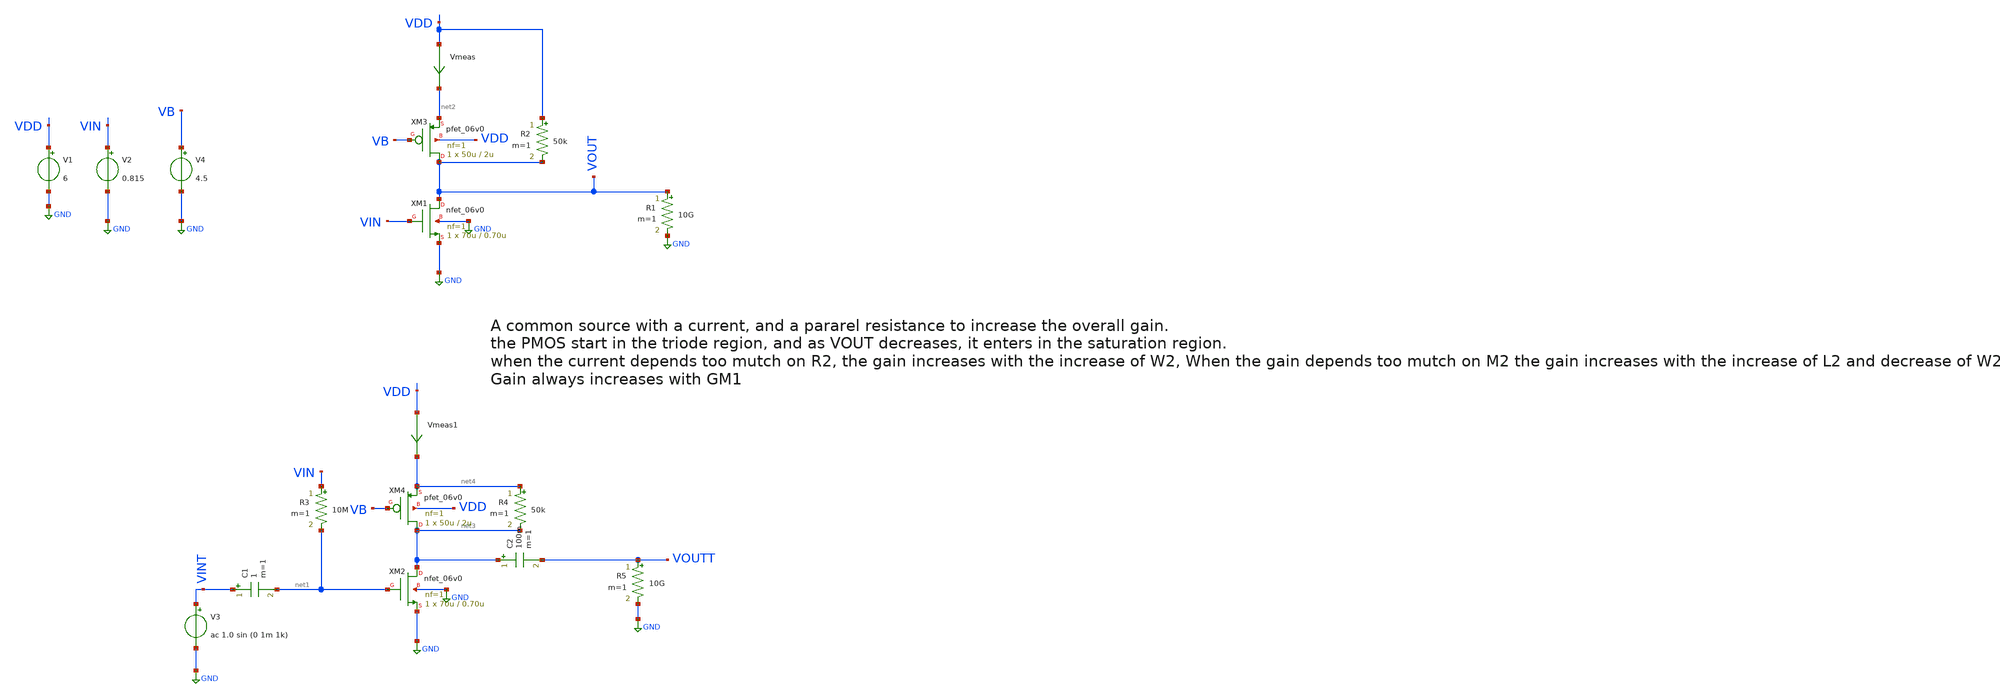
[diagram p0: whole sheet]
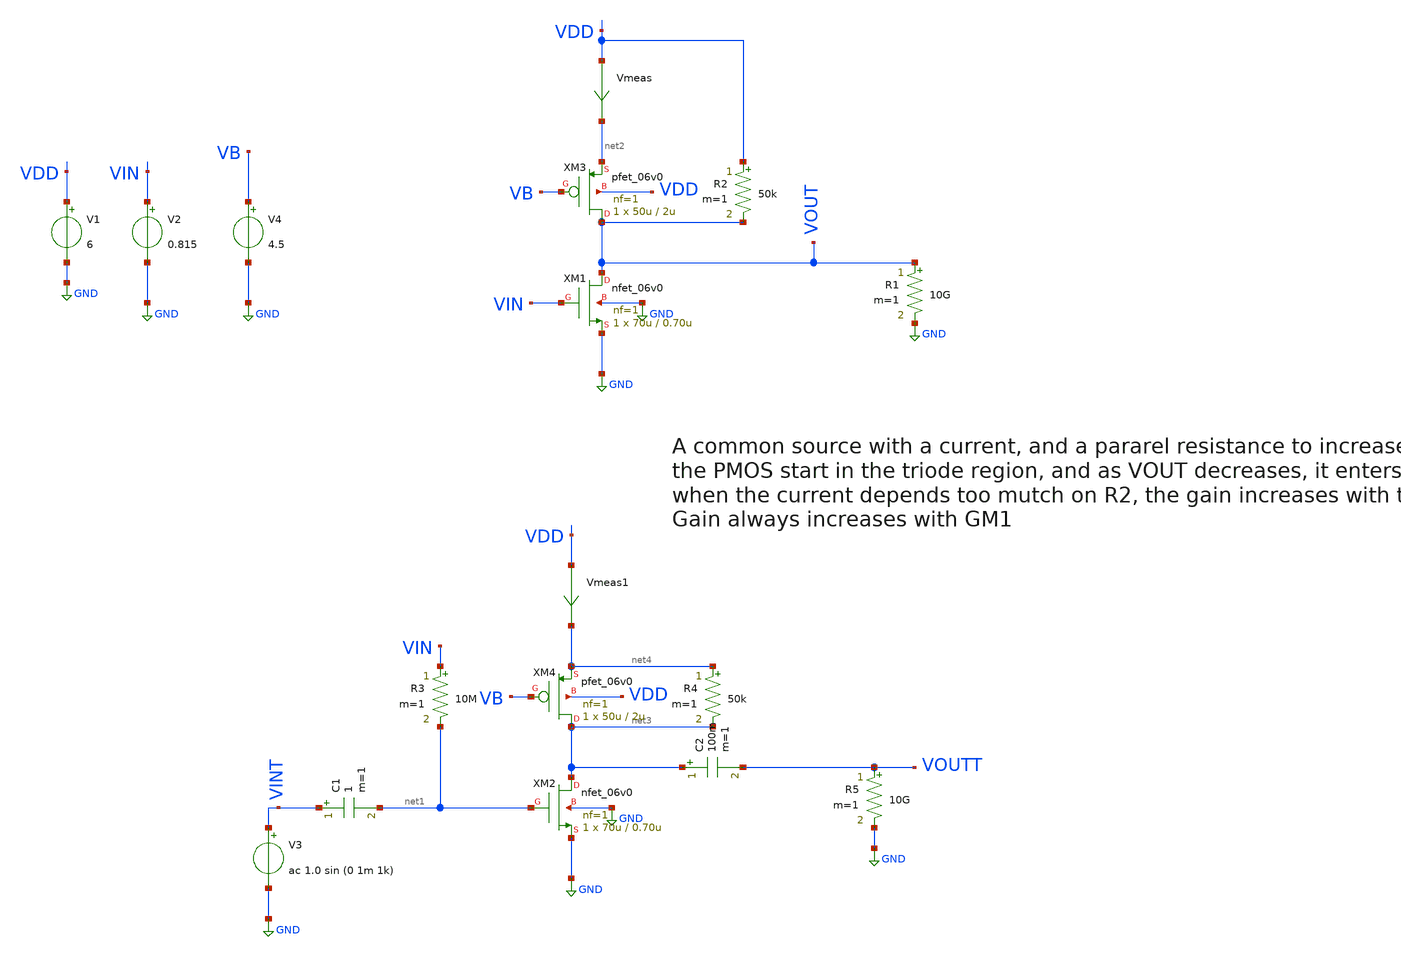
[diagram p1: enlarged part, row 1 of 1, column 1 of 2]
** sch_path: unusual_amplifiers/unusual_amp6.sch
**.subckt unusual_amp6
Vmeas VDD net2 0
.save i(vmeas)
V1 VDD GND 6
V2 VIN GND 0.815
V3 VINT GND ac 1.0 sin (0 1m 1k)
R3 VIN net1 10M m=1
R5 VOUTT GND 10G m=1
R1 VOUT GND 10G m=1
C1 VINT net1 1 m=1
XM1 VOUT VIN GND GND nfet_06v0 L=0.70u W=70u nf=1 ad='int((nf+1)/2) * W/nf * 0.18u' as='int((nf+2)/2) * W/nf * 0.18u'
+ pd='2*int((nf+1)/2) * (W/nf + 0.18u)' ps='2*int((nf+2)/2) * (W/nf + 0.18u)' nrd='0.18u / W' nrs='0.18u / W'
+ sa=0 sb=0 sd=0 m=1
R2 VDD VOUT 50k m=1
XM3 VOUT VB net2 VDD pfet_06v0 L=2u W=50u nf=1 ad='int((nf+1)/2) * W/nf * 0.18u' as='int((nf+2)/2) * W/nf * 0.18u'
+ pd='2*int((nf+1)/2) * (W/nf + 0.18u)' ps='2*int((nf+2)/2) * (W/nf + 0.18u)' nrd='0.18u / W' nrs='0.18u / W'
+ sa=0 sb=0 sd=0 m=1
V4 VB GND 4.5
Vmeas1 VDD net4 0
.save i(vmeas1)
XM4 net3 VB net4 VDD pfet_06v0 L=2u W=50u nf=1 ad='int((nf+1)/2) * W/nf * 0.18u' as='int((nf+2)/2) * W/nf * 0.18u'
+ pd='2*int((nf+1)/2) * (W/nf + 0.18u)' ps='2*int((nf+2)/2) * (W/nf + 0.18u)' nrd='0.18u / W' nrs='0.18u / W'
+ sa=0 sb=0 sd=0 m=1
R4 net4 net3 50k m=1
XM2 net3 net1 GND GND nfet_06v0 L=0.70u W=70u nf=1 ad='int((nf+1)/2) * W/nf * 0.18u' as='int((nf+2)/2) * W/nf * 0.18u'
+ pd='2*int((nf+1)/2) * (W/nf + 0.18u)' ps='2*int((nf+2)/2) * (W/nf + 0.18u)' nrd='0.18u / W' nrs='0.18u / W'
+ sa=0 sb=0 sd=0 m=1
C2 net3 VOUTT 100m m=1
**** begin user architecture code

**************************************************************
**************************************************************
**************************************************************
**************************************************************
**************************************************************
*LIBs*********************************************************
**************************************************************
**************************************************************
**************************************************************
**************************************************************
**************************************************************
.include $::180MCU_MODELS/design.ngspice
*.lib $::180MCU_MODELS/sm141064.ngspice statistical *use statistical if you want global and parameter mismatch
*.lib $::180MCU_MODELS/sm141064.ngspice res_statistical
.lib $::180MCU_MODELS/sm141064.ngspice typical
.lib $::180MCU_MODELS/sm141064.ngspice res_typical
.lib $::180MCU_MODELS/sm141064.ngspice moscap_typical
.lib $::180MCU_MODELS/sm141064.ngspice bjt_typical
.lib $::180MCU_MODELS/sm141064.ngspice diode_typical
.lib $::180MCU_MODELS/sm141064.ngspice mimcap_typical
**************************************************************
**************************************************************
**************************************************************
**************************************************************
**************************************************************
*Corners/montecarlo options***********************************
**************************************************************
**************************************************************
**************************************************************
**************************************************************
**************************************************************
.TEMP 27
.param   sw_stat_global = 1   sw_stat_mism = 1  mc_skew = 3  res_mc_skew = 3  cap_mc_skew = 3
+  fnoicor = 1
**************************************************************
**************************************************************
**************************************************************
**************************************************************
*SIMULATION and Plots*****************************************
**************************************************************
**************************************************************
**************************************************************
**************************************************************
.control
save all
dc V2 0 6 0.01
*dc simulation
plot v(VOUT) v(VIN) deriv(v(VOUT))
*ploting VIN VOUT and the voltage gain
plot i(Vmeas)
*ploting the current for curiosity
tran 100ns 2m
*transient simulation
plot (v(VINT)) (v(VOUTT))
*simple plot to exemplify the gain
fft v(VOUTT) v(VINT)
*fast fourier transfor
plot mag(v(VOUTT)) mag(v(VINT))
* analyse the frequency spectrum of the transient waves, to detect distortion
ac dec 20 1 50G
*simple ac simulation
plot v(VOUTT)
*gain in function of the input frequency
.endc

**** end user architecture code
**.ends
.GLOBAL GND
.end
